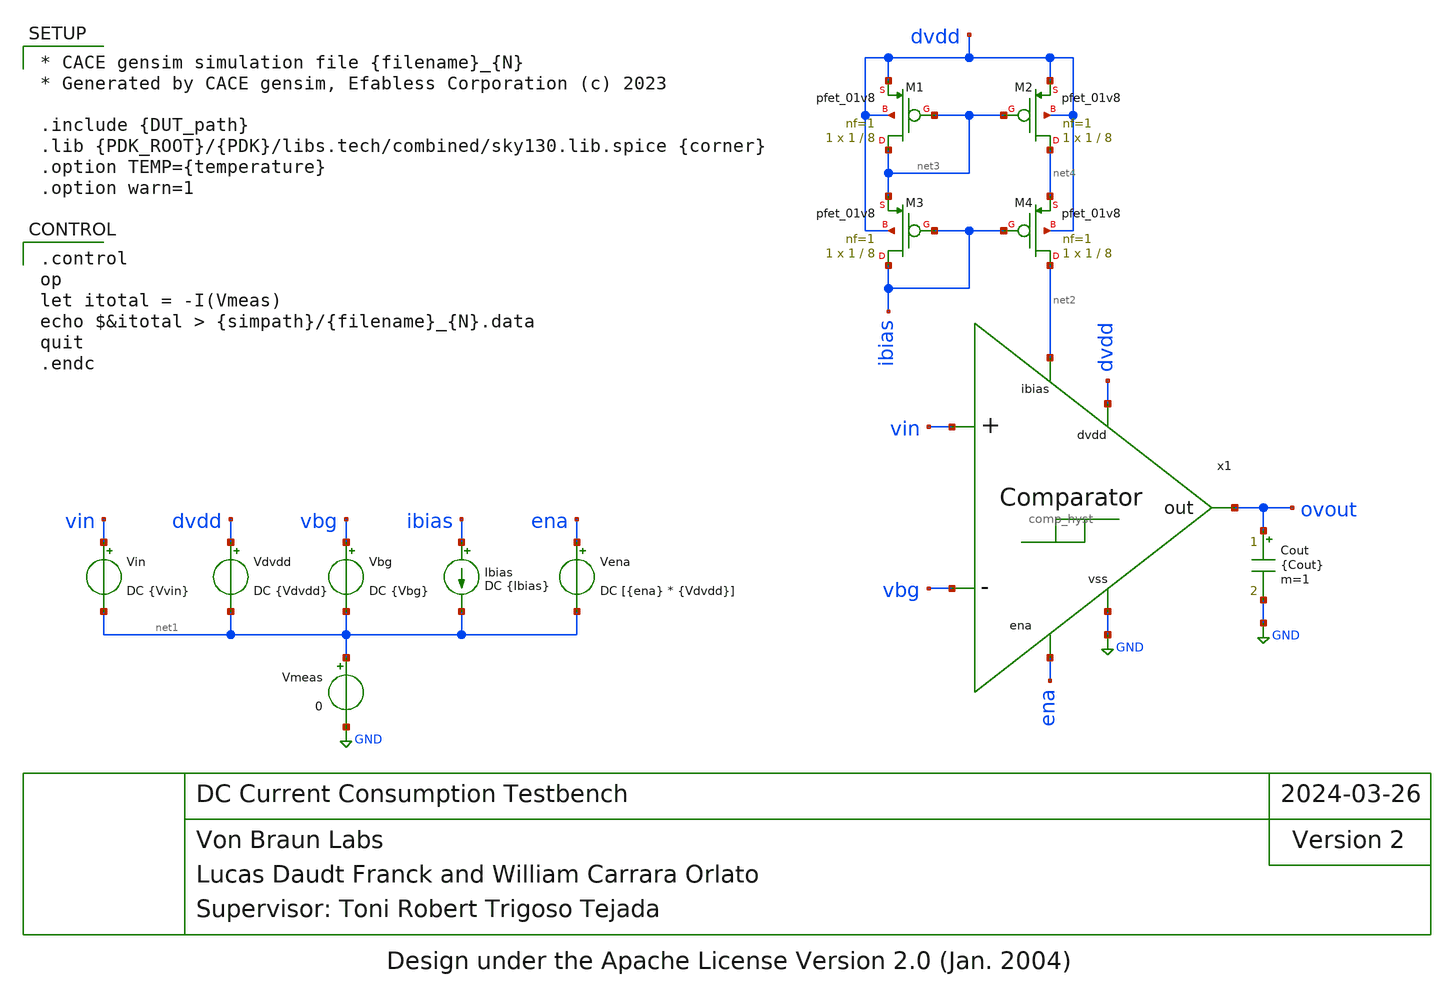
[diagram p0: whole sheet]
** sch_path: blocks/comp_hyst/cace/tb_dccurrent.sch
* Design under the Apache License Version 2.0 (Jan. 2004)
**.subckt tb_dccurrent
Cout ovout GND {Cout} m=1
Vin vin net1 DC {Vvin}
Vdvdd dvdd net1 DC {Vdvdd}
Vena ena net1 DC [{ena} * {Vdvdd}]
Vbg vbg net1 DC {Vbg}
Ibias ibias net1 DC {Ibias}
Vmeas net1 GND 0
XM1 net3 net3 dvdd dvdd sky130_fd_pr__pfet_01v8 L=8 W=1 nf=1 ad='int((nf+1)/2) * W/nf * 0.29' as='int((nf+2)/2) * W/nf * 0.29'
+ pd='2*int((nf+1)/2) * (W/nf + 0.29)' ps='2*int((nf+2)/2) * (W/nf + 0.29)' nrd='0.29 / W' nrs='0.29 / W'
+ sa=0 sb=0 sd=0 mult=1 m=1
XM2 net4 net3 dvdd dvdd sky130_fd_pr__pfet_01v8 L=8 W=1 nf=1 ad='int((nf+1)/2) * W/nf * 0.29' as='int((nf+2)/2) * W/nf * 0.29'
+ pd='2*int((nf+1)/2) * (W/nf + 0.29)' ps='2*int((nf+2)/2) * (W/nf + 0.29)' nrd='0.29 / W' nrs='0.29 / W'
+ sa=0 sb=0 sd=0 mult=1 m=1
XM3 ibias ibias net3 dvdd sky130_fd_pr__pfet_01v8 L=8 W=1 nf=1 ad='int((nf+1)/2) * W/nf * 0.29' as='int((nf+2)/2) * W/nf * 0.29'
+ pd='2*int((nf+1)/2) * (W/nf + 0.29)' ps='2*int((nf+2)/2) * (W/nf + 0.29)' nrd='0.29 / W' nrs='0.29 / W'
+ sa=0 sb=0 sd=0 mult=1 m=1
XM4 net2 ibias net4 dvdd sky130_fd_pr__pfet_01v8 L=8 W=1 nf=1 ad='int((nf+1)/2) * W/nf * 0.29' as='int((nf+2)/2) * W/nf * 0.29'
+ pd='2*int((nf+1)/2) * (W/nf + 0.29)' ps='2*int((nf+2)/2) * (W/nf + 0.29)' nrd='0.29 / W' nrs='0.29 / W'
+ sa=0 sb=0 sd=0 mult=1 m=1
x1 dvdd ovout vbg vin ena net2 GND comp_hyst
**** begin user architecture code

* CACE gensim simulation file {filename}_{N}
* Generated by CACE gensim, Efabless Corporation (c) 2023

.include {DUT_path}
.lib {PDK_ROOT}/{PDK}/libs.tech/combined/sky130.lib.spice {corner}
.option TEMP={temperature}
.option warn=1



.control
op
let itotal = -I(Vmeas)
echo $&itotal > {simpath}/{filename}_{N}.data
quit
.endc


**** end user architecture code
**.ends
.GLOBAL GND
.end
